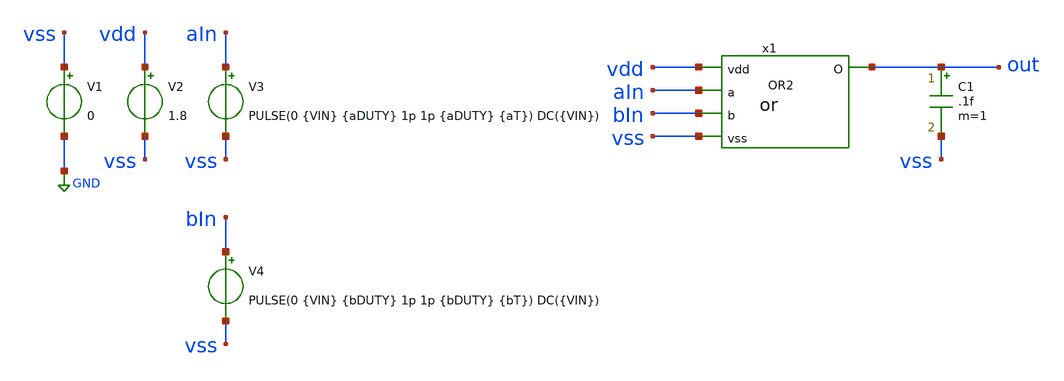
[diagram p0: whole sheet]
** sch_path: eamta2021/sch/or/tbOr.sch
**.subckt tbOr
V1 vss GND 0
V2 vdd vss 1.8
V3 aIn vss PULSE(0 {VIN} {aDUTY} 1p 1p {aDUTY} {aT}) DC({VIN})
C1 out vss .1f m=1
V4 bIn vss PULSE(0 {VIN} {bDUTY} 1p 1p {bDUTY} {bT}) DC({VIN})
x1 vdd aIn out bIn vss or
**** begin user architecture code



* parametros
.param VIN=1.8 aT=100n aDUTY=50n bT=100n bDUTY=50n WN=.450 WP=.90
.options TEMP=27.0

* include corners
.lib /home/eamta/skywater/skywater-pdk/libraries/sky130_fd_pr_ngspice/latest/models/corners/sky130.lib TT

* saves
.save all
**PFETs  @M.x1.xm1.msky130_fd_pr__pfet_01v8[id]  @M.x1.xm1.msky130_fd_pr__pfet_01v8[vds]
*+  @M.x1.xm1.msky130_fd_pr__pfet_01v8[vgs]  @M.x1.xm1.msky130_fd_pr__pfet_01v8[vth]  @M.x1.xm2.msky130_fd_pr__pfet_01v8[id]
*+  @M.x1.xm2.msky130_fd_pr__pfet_01v8[vds]  @M.x1.xm2.msky130_fd_pr__pfet_01v8[vgs]  @M.x1.xm2.msky130_fd_pr__pfet_01v8[vth]
*+  @M.x1.xm5.msky130_fd_pr__pfet_01v8[id]  @M.x1.xm5.msky130_fd_pr__pfet_01v8[vds]  @M.x1.xm5.msky130_fd_pr__pfet_01v8[vgs]
*+  @M.x1.xm5.msky130_fd_pr__pfet_01v8[vth]
**NFETs  @M.x1.xm3.msky130_fd_pr__nfet_01v8[id]  @M.x1.xm3.msky130_fd_pr__nfet_01v8[vds]
*+  @M.x1.xm3.msky130_fd_pr__nfet_01v8[vgs]  @M.x1.xm3.msky130_fd_pr__nfet_01v8[vth]  @M.x1.xm4.msky130_fd_pr__nfet_01v8[id]
*+  @M.x1.xm4.msky130_fd_pr__nfet_01v8[vds]  @M.x1.xm4.msky130_fd_pr__nfet_01v8[vgs]  @M.x1.xm4.msky130_fd_pr__nfet_01v8[vth]
*+  @M.x1.xm6.msky130_fd_pr__nfet_01v8[id]  @M.x1.xm6.msky130_fd_pr__nfet_01v8[vds]  @M.x1.xm6.msky130_fd_pr__nfet_01v8[vgs]
*+  @M.x1.xm6.msky130_fd_pr__nfet_01v8[vth]

* SIM
.control
	******************************************************
	*let At=.005ns

	tran 0.005ns 500ns

	setplot tran1
	**comportamiento
	*plot v(aIn) v(bIn)+2 v(out)+4
	**rise/fall
	plot v(out) v(aIn) .18 1.62 xlimit 99.95ns 100.15ns
	plot v(out) v(aIn) .18 1.62 xlimit 149.999ns 150.020ns
	**sos inimputable
	*plot tran1.@M.x1.xm1.msky130_fd_pr__nfet_01v8[vds]
	*plot tran1.@M.x1.xm1.msky130_fd_pr__nfet_01v8[id] tran1.@M.x1.xm2.msky130_fd_pr__pfet_01v8[id]

	*set filetype=ascii
	*write simInvTran.raw
	*reset
	******************************************************
	*alterparam bDUTY=100n
	*dc V3 0 1.8 0.01
	*alterparam aDUTY=100n
	*dc V4 0 1.8 0.01
	*dc V3 0 1.8 0.01 V4 0 1.8 0.01

	*setplot dc1
	*plot dc1.out vs dc1.aIn dc2.out vs dc2.bIn dc3.out vs dc3.aIn
	*plot @M.x1.xm1.msky130_fd_pr__nfet_01v8[id]
	*plot @M.x1.xm1.msky130_fd_pr__nfet_01v8[vd]

	*set filetype=ascii
	*write simInvDc.raw
	*reset
	******************************************************
	op

	set filetype=ascii
	write simInvOp.raw
	reset

***********************************************************
	*analisis cuasi parametrico
	*tran 0.001ns 200ns

	*alterparam WP=1.35
	*tran 0.001ns 200ns

	*alterparam WP=1.5
	*tran 0.001ns 200ns

	*plot tran1.out tran2.out tran3.out v(aIn) .18 1.62 xlimit 99.95ns 100.15ns
	*plot tran1.out tran2.out tran3.out v(aIn) .18 1.62 xlimit 149.999ns 150.020ns

	print all
.endc

.end


**** end user architecture code
**.ends

* expanding   symbol:  or/or.sym # of pins=5
** sym_path: eamta2021/sch/or/or.sym
** sch_path: eamta2021/sch/or/or.sch
.subckt or vdd a O b vss
*.ipin vdd
*.ipin a
*.ipin b
*.ipin vss
*.opin O
XM1 net2 a vdd vdd sky130_fd_pr__pfet_01v8 L=0.15 W={WP} nf=1 ad='int((nf+1)/2) * W/nf * 0.29' as='int((nf+2)/2) * W/nf * 0.29'
+ pd='2*int((nf+1)/2) * (W/nf + 0.29)' ps='2*int((nf+2)/2) * (W/nf + 0.29)' nrd='0.29 / W' nrs='0.29 / W'
+ sa=0 sb=0 sd=0 mult=1 m=1
XM2 net1 b net2 vdd sky130_fd_pr__pfet_01v8 L=0.15 W={WP} nf=1 ad='int((nf+1)/2) * W/nf * 0.29' as='int((nf+2)/2) * W/nf * 0.29'
+ pd='2*int((nf+1)/2) * (W/nf + 0.29)' ps='2*int((nf+2)/2) * (W/nf + 0.29)' nrd='0.29 / W' nrs='0.29 / W'
+ sa=0 sb=0 sd=0 mult=1 m=1
XM3 net1 b vss vss sky130_fd_pr__nfet_01v8 L=0.15 W={WN} nf=1 ad='int((nf+1)/2) * W/nf * 0.29' as='int((nf+2)/2) * W/nf * 0.29'
+ pd='2*int((nf+1)/2) * (W/nf + 0.29)' ps='2*int((nf+2)/2) * (W/nf + 0.29)' nrd='0.29 / W' nrs='0.29 / W'
+ sa=0 sb=0 sd=0 mult=1 m=1
XM4 net1 a vss vss sky130_fd_pr__nfet_01v8 L=0.15 W={WN} nf=1 ad='int((nf+1)/2) * W/nf * 0.29' as='int((nf+2)/2) * W/nf * 0.29'
+ pd='2*int((nf+1)/2) * (W/nf + 0.29)' ps='2*int((nf+2)/2) * (W/nf + 0.29)' nrd='0.29 / W' nrs='0.29 / W'
+ sa=0 sb=0 sd=0 mult=1 m=1
XM5 O net1 vdd vdd sky130_fd_pr__pfet_01v8 L=0.15 W={WP} nf=1 ad='int((nf+1)/2) * W/nf * 0.29' as='int((nf+2)/2) * W/nf * 0.29'
+ pd='2*int((nf+1)/2) * (W/nf + 0.29)' ps='2*int((nf+2)/2) * (W/nf + 0.29)' nrd='0.29 / W' nrs='0.29 / W'
+ sa=0 sb=0 sd=0 mult=1 m=1
XM6 O net1 vss vss sky130_fd_pr__nfet_01v8 L=0.15 W={WN} nf=1 ad='int((nf+1)/2) * W/nf * 0.29' as='int((nf+2)/2) * W/nf * 0.29'
+ pd='2*int((nf+1)/2) * (W/nf + 0.29)' ps='2*int((nf+2)/2) * (W/nf + 0.29)' nrd='0.29 / W' nrs='0.29 / W'
+ sa=0 sb=0 sd=0 mult=1 m=1
.ends

.GLOBAL GND
.end
